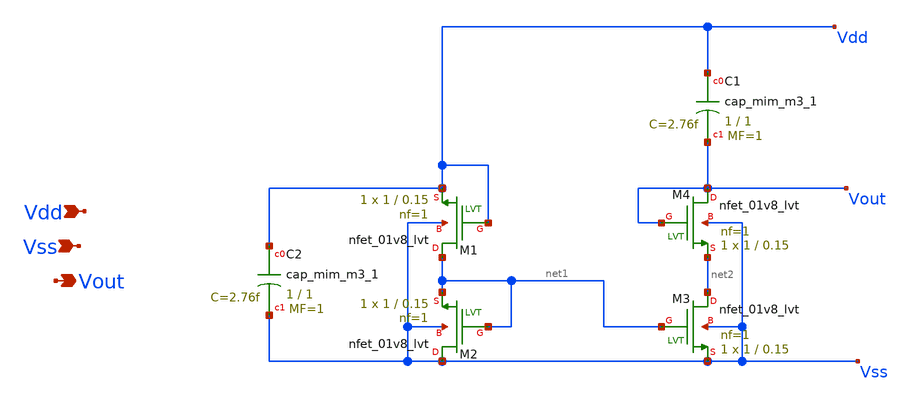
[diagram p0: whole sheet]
** sch_path: tt10-hdl/tt_um_test_commit/xschem/T2/startup/POR/Z_old/2cap-4fet-molnar2018_por.sch
**.subckt 2cap-4fet-molnar2018_por Vdd Vss Vout
*.ipin Vdd
*.ipin Vss
*.opin Vout
XM1 net1 Vdd Vdd Vss sky130_fd_pr__nfet_01v8_lvt L=0.15 W=1 nf=1 ad='int((1 + 1)/2) * 1 / 1 * 0.29' as='int((1 + 2)/2) * 1 / 1 * 0.29'
+ pd='2*int((1 + 1)/2) * (1 / 1 + 0.29)' ps='2*int((1 + 2)/2) * (1 / 1 + 0.29)' nrd='0.29 / 1 ' nrs='0.29 / 1 '
+ sa=0 sb=0 sd=0 mult=1 m=1
XM2 Vss net1 net1 Vss sky130_fd_pr__nfet_01v8_lvt L=0.15 W=1 nf=1 ad='int((1 + 1)/2) * 1 / 1 * 0.29'
+ as='int((1 + 2)/2) * 1 / 1 * 0.29' pd='2*int((1 + 1)/2) * (1 / 1 + 0.29)' ps='2*int((1 + 2)/2) * (1 / 1 + 0.29)'
+ nrd='0.29 / 1 ' nrs='0.29 / 1 ' sa=0 sb=0 sd=0 mult=1 m=1
XM3 net2 net1 Vss Vss sky130_fd_pr__nfet_01v8_lvt L=0.15 W=1 nf=1 ad='int((1 + 1)/2) * 1 / 1 * 0.29'
+ as='int((1 + 2)/2) * 1 / 1 * 0.29' pd='2*int((1 + 1)/2) * (1 / 1 + 0.29)' ps='2*int((1 + 2)/2) * (1 / 1 + 0.29)'
+ nrd='0.29 / 1 ' nrs='0.29 / 1 ' sa=0 sb=0 sd=0 mult=1 m=1
XM4 Vout Vout net2 Vss sky130_fd_pr__nfet_01v8_lvt L=0.15 W=1 nf=1 ad='int((1 + 1)/2) * 1 / 1 * 0.29'
+ as='int((1 + 2)/2) * 1 / 1 * 0.29' pd='2*int((1 + 1)/2) * (1 / 1 + 0.29)' ps='2*int((1 + 2)/2) * (1 / 1 + 0.29)'
+ nrd='0.29 / 1 ' nrs='0.29 / 1 ' sa=0 sb=0 sd=0 mult=1 m=1
XC1 Vdd Vout sky130_fd_pr__cap_mim_m3_1 W=1 L=1 MF=1 m=1
XC2 Vdd Vss sky130_fd_pr__cap_mim_m3_1 W=1 L=1 MF=1 m=1
**.ends
.end
